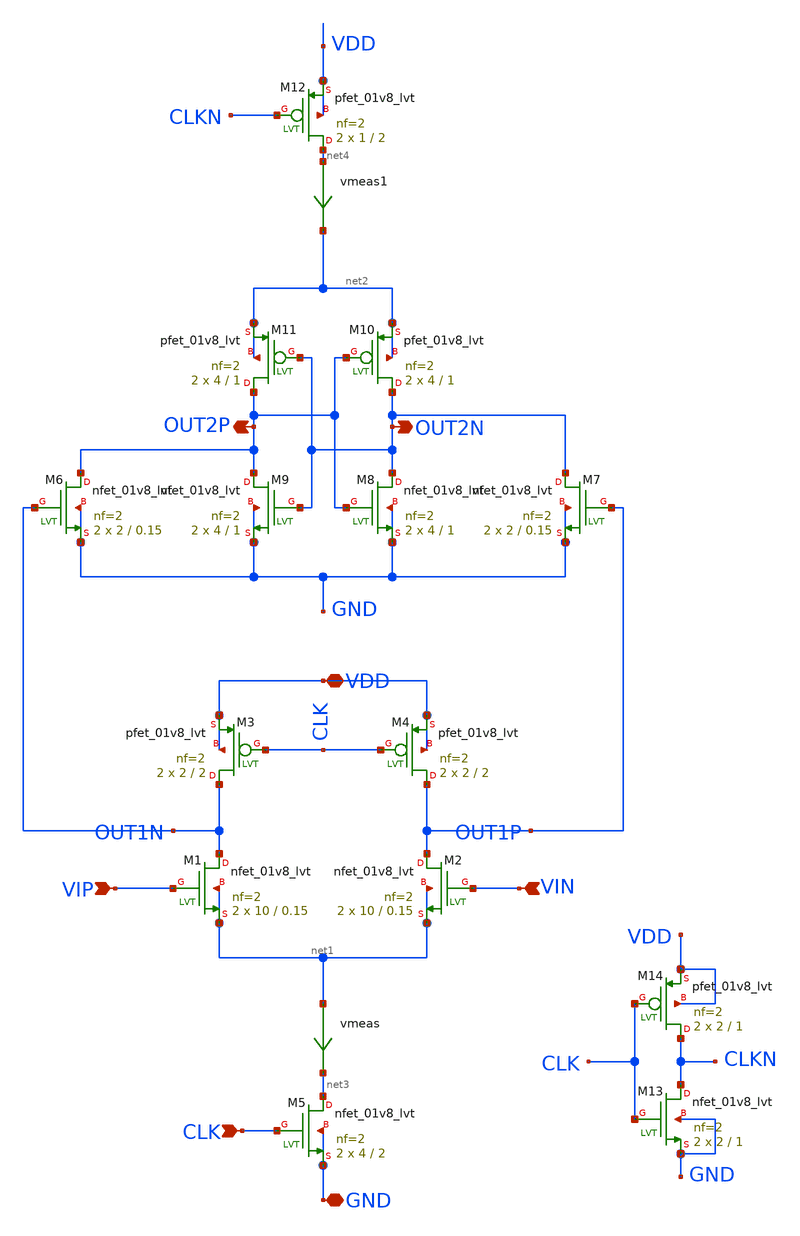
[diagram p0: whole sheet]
** sch_path: xschem/UL_C_schematic.sch
**.subckt UL_C_schematic VIP VIN CLK GND OUT2N OUT2P VDD
*.ipin VIP
*.ipin VIN
*.ipin CLK
*.iopin GND
*.opin OUT2N
*.opin OUT2P
*.iopin VDD
XM1 OUT1N VIP net1 net1 sky130_fd_pr__nfet_01v8_lvt L=0.15 W=10 nf=2 ad='int((nf+1)/2) * W/nf * 0.29'
+ as='int((nf+2)/2) * W/nf * 0.29' pd='2*int((nf+1)/2) * (W/nf + 0.29)' ps='2*int((nf+2)/2) * (W/nf + 0.29)'
+ nrd='0.29 / W' nrs='0.29 / W' sa=0 sb=0 sd=0 mult=2 m=2
XM2 OUT1P VIN net1 net1 sky130_fd_pr__nfet_01v8_lvt L=0.15 W=10 nf=2 ad='int((nf+1)/2) * W/nf * 0.29'
+ as='int((nf+2)/2) * W/nf * 0.29' pd='2*int((nf+1)/2) * (W/nf + 0.29)' ps='2*int((nf+2)/2) * (W/nf + 0.29)'
+ nrd='0.29 / W' nrs='0.29 / W' sa=0 sb=0 sd=0 mult=2 m=2
XM3 OUT1N CLK VDD VDD sky130_fd_pr__pfet_01v8_lvt L=2 W=2 nf=2 ad='int((nf+1)/2) * W/nf * 0.29' as='int((nf+2)/2) * W/nf * 0.29'
+ pd='2*int((nf+1)/2) * (W/nf + 0.29)' ps='2*int((nf+2)/2) * (W/nf + 0.29)' nrd='0.29 / W' nrs='0.29 / W'
+ sa=0 sb=0 sd=0 mult=2 m=2
XM4 OUT1P CLK VDD VDD sky130_fd_pr__pfet_01v8_lvt L=2 W=2 nf=2 ad='int((nf+1)/2) * W/nf * 0.29' as='int((nf+2)/2) * W/nf * 0.29'
+ pd='2*int((nf+1)/2) * (W/nf + 0.29)' ps='2*int((nf+2)/2) * (W/nf + 0.29)' nrd='0.29 / W' nrs='0.29 / W'
+ sa=0 sb=0 sd=0 mult=2 m=2
XM5 net3 CLK GND GND sky130_fd_pr__nfet_01v8_lvt L=2 W=4 nf=2 ad='int((nf+1)/2) * W/nf * 0.29' as='int((nf+2)/2) * W/nf * 0.29'
+ pd='2*int((nf+1)/2) * (W/nf + 0.29)' ps='2*int((nf+2)/2) * (W/nf + 0.29)' nrd='0.29 / W' nrs='0.29 / W'
+ sa=0 sb=0 sd=0 mult=2 m=2
XM6 OUT2P OUT1N GND GND sky130_fd_pr__nfet_01v8_lvt L=0.15 W=2 nf=2 ad='int((nf+1)/2) * W/nf * 0.29'
+ as='int((nf+2)/2) * W/nf * 0.29' pd='2*int((nf+1)/2) * (W/nf + 0.29)' ps='2*int((nf+2)/2) * (W/nf + 0.29)'
+ nrd='0.29 / W' nrs='0.29 / W' sa=0 sb=0 sd=0 mult=2 m=2
XM7 OUT2N OUT1P GND GND sky130_fd_pr__nfet_01v8_lvt L=0.15 W=2 nf=2 ad='int((nf+1)/2) * W/nf * 0.29'
+ as='int((nf+2)/2) * W/nf * 0.29' pd='2*int((nf+1)/2) * (W/nf + 0.29)' ps='2*int((nf+2)/2) * (W/nf + 0.29)'
+ nrd='0.29 / W' nrs='0.29 / W' sa=0 sb=0 sd=0 mult=2 m=2
XM8 OUT2N OUT2P GND GND sky130_fd_pr__nfet_01v8_lvt L=1 W=4 nf=2 ad='int((nf+1)/2) * W/nf * 0.29' as='int((nf+2)/2) * W/nf * 0.29'
+ pd='2*int((nf+1)/2) * (W/nf + 0.29)' ps='2*int((nf+2)/2) * (W/nf + 0.29)' nrd='0.29 / W' nrs='0.29 / W'
+ sa=0 sb=0 sd=0 mult=2 m=2
XM9 OUT2P OUT2N GND GND sky130_fd_pr__nfet_01v8_lvt L=1 W=4 nf=2 ad='int((nf+1)/2) * W/nf * 0.29' as='int((nf+2)/2) * W/nf * 0.29'
+ pd='2*int((nf+1)/2) * (W/nf + 0.29)' ps='2*int((nf+2)/2) * (W/nf + 0.29)' nrd='0.29 / W' nrs='0.29 / W'
+ sa=0 sb=0 sd=0 mult=2 m=2
XM10 OUT2N OUT2P net2 net2 sky130_fd_pr__pfet_01v8_lvt L=1 W=4 nf=2 ad='int((nf+1)/2) * W/nf * 0.29'
+ as='int((nf+2)/2) * W/nf * 0.29' pd='2*int((nf+1)/2) * (W/nf + 0.29)' ps='2*int((nf+2)/2) * (W/nf + 0.29)'
+ nrd='0.29 / W' nrs='0.29 / W' sa=0 sb=0 sd=0 mult=2 m=2
XM11 OUT2P OUT2N net2 net2 sky130_fd_pr__pfet_01v8_lvt L=1 W=4 nf=2 ad='int((nf+1)/2) * W/nf * 0.29'
+ as='int((nf+2)/2) * W/nf * 0.29' pd='2*int((nf+1)/2) * (W/nf + 0.29)' ps='2*int((nf+2)/2) * (W/nf + 0.29)'
+ nrd='0.29 / W' nrs='0.29 / W' sa=0 sb=0 sd=0 mult=2 m=2
XM12 net4 CLKN VDD VDD sky130_fd_pr__pfet_01v8_lvt L=2 W=1 nf=2 ad='int((nf+1)/2) * W/nf * 0.29' as='int((nf+2)/2) * W/nf * 0.29'
+ pd='2*int((nf+1)/2) * (W/nf + 0.29)' ps='2*int((nf+2)/2) * (W/nf + 0.29)' nrd='0.29 / W' nrs='0.29 / W'
+ sa=0 sb=0 sd=0 mult=2 m=2
vmeas net1 net3 0
.save i(vmeas)
vmeas1 net4 net2 0
.save i(vmeas1)
XM13 CLKN CLK GND GND sky130_fd_pr__nfet_01v8_lvt L=1 W=2 nf=2 ad='int((nf+1)/2) * W/nf * 0.29' as='int((nf+2)/2) * W/nf * 0.29'
+ pd='2*int((nf+1)/2) * (W/nf + 0.29)' ps='2*int((nf+2)/2) * (W/nf + 0.29)' nrd='0.29 / W' nrs='0.29 / W'
+ sa=0 sb=0 sd=0 mult=2 m=2
XM14 CLKN CLK VDD VDD sky130_fd_pr__pfet_01v8_lvt L=1 W=2 nf=2 ad='int((nf+1)/2) * W/nf * 0.29' as='int((nf+2)/2) * W/nf * 0.29'
+ pd='2*int((nf+1)/2) * (W/nf + 0.29)' ps='2*int((nf+2)/2) * (W/nf + 0.29)' nrd='0.29 / W' nrs='0.29 / W'
+ sa=0 sb=0 sd=0 mult=2 m=2
**.ends
.end
